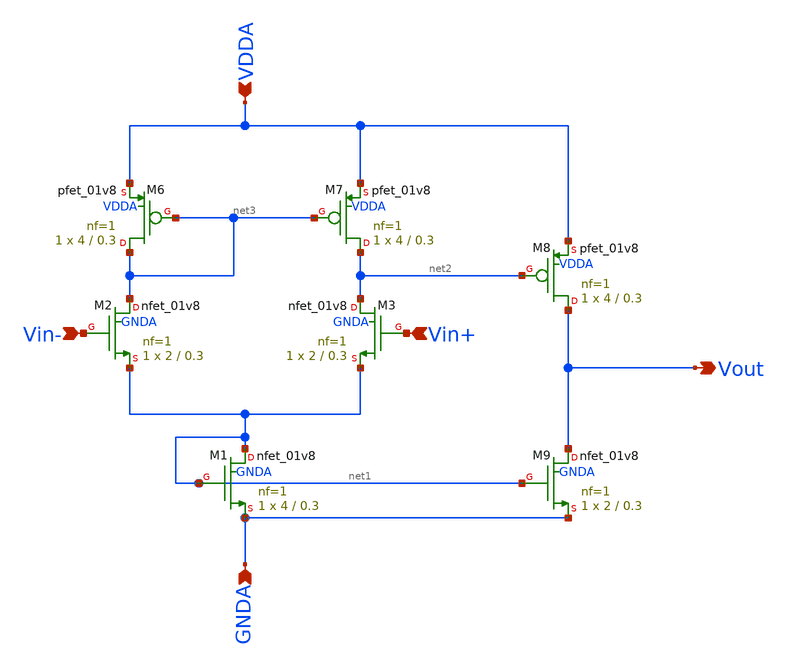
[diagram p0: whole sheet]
** sch_path: projects/pll/bandgapref/xschem_ngspice/opamp_bandgap.sch
**.subckt opamp_bandgap Vin- Vout Vin+ GNDA VDDA
*.ipin Vin-
*.opin Vout
*.ipin Vin+
*.ipin GNDA
*.ipin VDDA
XM2 net3 Vin- net1 GNDA sky130_fd_pr__nfet_01v8 L=0.3 W=2 nf=1 ad='int((nf+1)/2) * W/nf * 0.29' as='int((nf+2)/2) * W/nf * 0.29'
+ pd='2*int((nf+1)/2) * (W/nf + 0.29)' ps='2*int((nf+2)/2) * (W/nf + 0.29)' nrd='0.29 / W' nrs='0.29 / W'
+ sa=0 sb=0 sd=0 mult=1 m=1
XM3 net2 Vin+ net1 GNDA sky130_fd_pr__nfet_01v8 L=0.3 W=2 nf=1 ad='int((nf+1)/2) * W/nf * 0.29' as='int((nf+2)/2) * W/nf * 0.29'
+ pd='2*int((nf+1)/2) * (W/nf + 0.29)' ps='2*int((nf+2)/2) * (W/nf + 0.29)' nrd='0.29 / W' nrs='0.29 / W'
+ sa=0 sb=0 sd=0 mult=1 m=1
XM1 net1 net1 GNDA GNDA sky130_fd_pr__nfet_01v8 L=0.3 W=4 nf=1 ad='int((nf+1)/2) * W/nf * 0.29' as='int((nf+2)/2) * W/nf * 0.29'
+ pd='2*int((nf+1)/2) * (W/nf + 0.29)' ps='2*int((nf+2)/2) * (W/nf + 0.29)' nrd='0.29 / W' nrs='0.29 / W'
+ sa=0 sb=0 sd=0 mult=1 m=1
XM6 net3 net3 VDDA VDDA sky130_fd_pr__pfet_01v8 L=0.3 W=4 nf=1 ad='int((nf+1)/2) * W/nf * 0.29' as='int((nf+2)/2) * W/nf * 0.29'
+ pd='2*int((nf+1)/2) * (W/nf + 0.29)' ps='2*int((nf+2)/2) * (W/nf + 0.29)' nrd='0.29 / W' nrs='0.29 / W'
+ sa=0 sb=0 sd=0 mult=1 m=1
XM7 net2 net3 VDDA VDDA sky130_fd_pr__pfet_01v8 L=0.3 W=4 nf=1 ad='int((nf+1)/2) * W/nf * 0.29' as='int((nf+2)/2) * W/nf * 0.29'
+ pd='2*int((nf+1)/2) * (W/nf + 0.29)' ps='2*int((nf+2)/2) * (W/nf + 0.29)' nrd='0.29 / W' nrs='0.29 / W'
+ sa=0 sb=0 sd=0 mult=1 m=1
XM8 Vout net2 VDDA VDDA sky130_fd_pr__pfet_01v8 L=0.3 W=4 nf=1 ad='int((nf+1)/2) * W/nf * 0.29' as='int((nf+2)/2) * W/nf * 0.29'
+ pd='2*int((nf+1)/2) * (W/nf + 0.29)' ps='2*int((nf+2)/2) * (W/nf + 0.29)' nrd='0.29 / W' nrs='0.29 / W'
+ sa=0 sb=0 sd=0 mult=1 m=1
XM9 Vout net1 GNDA GNDA sky130_fd_pr__nfet_01v8 L=0.3 W=2 nf=1 ad='int((nf+1)/2) * W/nf * 0.29' as='int((nf+2)/2) * W/nf * 0.29'
+ pd='2*int((nf+1)/2) * (W/nf + 0.29)' ps='2*int((nf+2)/2) * (W/nf + 0.29)' nrd='0.29 / W' nrs='0.29 / W'
+ sa=0 sb=0 sd=0 mult=1 m=1
**.ends
.end
